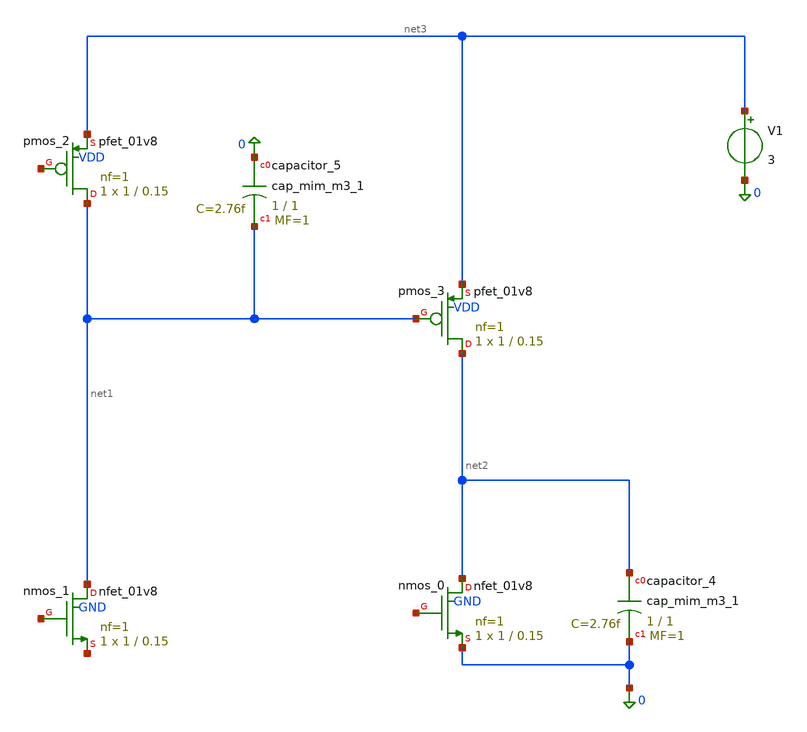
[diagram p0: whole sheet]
** sch_path: golden_netlists/10_1007_s00034-017-0630-6_05_001_crop1.sch
**.subckt 10_1007_s00034-017-0630-6_05_001_crop1
Xcapacitor_4 net2 0 sky130_fd_pr__cap_mim_m3_1 W=1 L=1 MF=1 m=1
Xcapacitor_5 0 net1 sky130_fd_pr__cap_mim_m3_1 W=1 L=1 MF=1 m=1
Xnmos_0 net2 net4 0 GND sky130_fd_pr__nfet_01v8 L=0.15 W=1 nf=1 ad='int((nf+1)/2) * W/nf * 0.29' as='int((nf+2)/2) * W/nf * 0.29'
+ pd='2*int((nf+1)/2) * (W/nf + 0.29)' ps='2*int((nf+2)/2) * (W/nf + 0.29)' nrd='0.29 / W' nrs='0.29 / W'
+ sa=0 sb=0 sd=0 mult=1 m=1
Xnmos_1 net1 net5 net6 GND sky130_fd_pr__nfet_01v8 L=0.15 W=1 nf=1 ad='int((nf+1)/2) * W/nf * 0.29' as='int((nf+2)/2) * W/nf * 0.29'
+ pd='2*int((nf+1)/2) * (W/nf + 0.29)' ps='2*int((nf+2)/2) * (W/nf + 0.29)' nrd='0.29 / W' nrs='0.29 / W'
+ sa=0 sb=0 sd=0 mult=1 m=1
Xpmos_2 net1 net7 net3 VDD sky130_fd_pr__pfet_01v8 L=0.15 W=1 nf=1 ad='int((1 + 1)/2) * 1 / 1 * 0.29'
+ as='int((1 + 2)/2) * 1 / 1 * 0.29' pd='2*int((1 + 1)/2) * (1 / 1 + 0.29)' ps='2*int((1 + 2)/2) * (1 / 1 + 0.29)'
+ nrd='0.29 / 1 ' nrs='0.29 / 1 ' sa=0 sb=0 sd=0 mult=1 m=1
Xpmos_3 net2 net1 net3 VDD sky130_fd_pr__pfet_01v8 L=0.15 W=1 nf=1 ad='int((1 + 1)/2) * 1 / 1 * 0.29'
+ as='int((1 + 2)/2) * 1 / 1 * 0.29' pd='2*int((1 + 1)/2) * (1 / 1 + 0.29)' ps='2*int((1 + 2)/2) * (1 / 1 + 0.29)'
+ nrd='0.29 / 1 ' nrs='0.29 / 1 ' sa=0 sb=0 sd=0 mult=1 m=1
V1 net3 0 3
**.ends
.end
